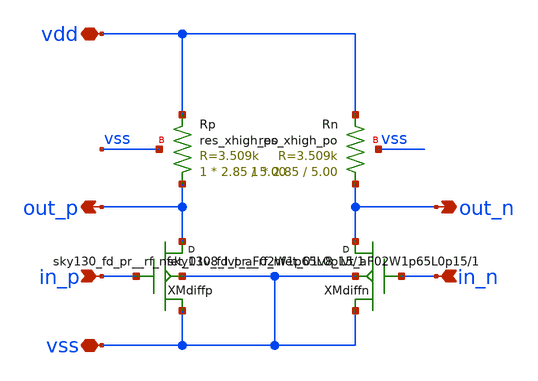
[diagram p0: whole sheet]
** sch_path: design/rf_bufferdiff/rf_bufferdiff.sch
**.subckt rf_bufferdiff vdd vss in_p in_n out_p out_n
*.iopin vdd
*.iopin vss
*.ipin in_p
*.ipin in_n
*.opin out_p
*.opin out_n
XXMdiffp out_p in_p vss vss sky130_fd_pr__rf_nfet_01v8_lvt_aF02W1p65L0p15 m=1
XXMdiffn out_n in_n vss vss sky130_fd_pr__rf_nfet_01v8_lvt_aF02W1p65L0p15 m=1
XRp out_p vdd vss sky130_fd_pr__res_xhigh_po W=2.85 L=5.00 mult=1 m=1
XRn out_n vdd vss sky130_fd_pr__res_xhigh_po W=2.85 L=5.00 mult=1 m=1
**.ends
.end
